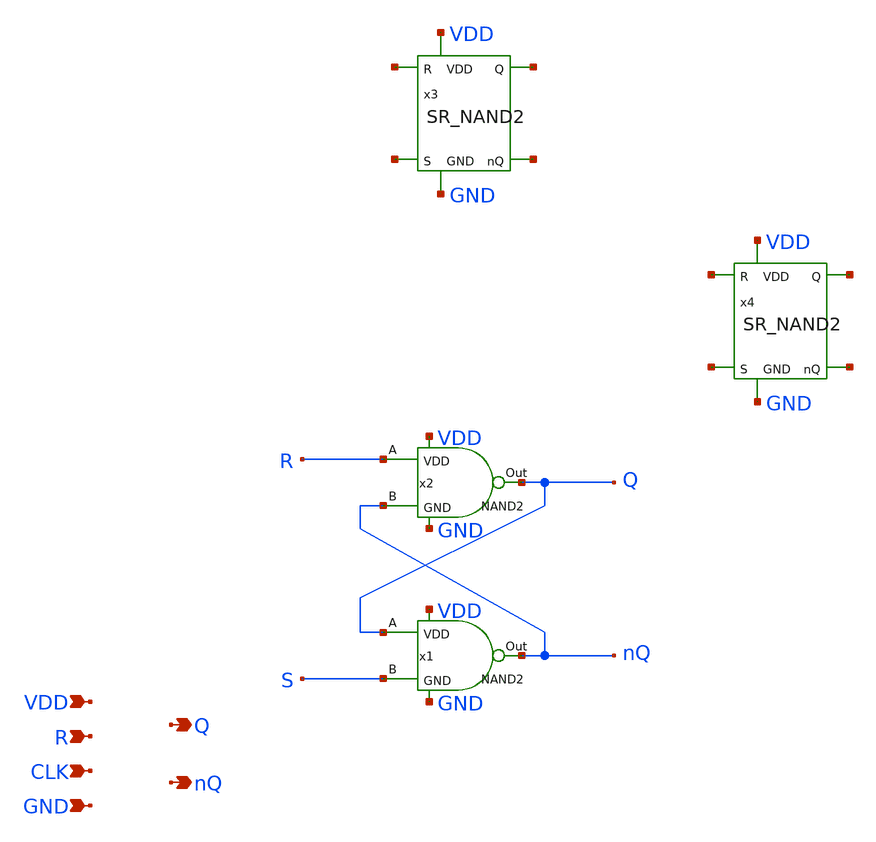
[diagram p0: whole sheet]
** sch_path: src/Dff.sch
**.subckt Dff Q R CLK VDD GND nQ
*.opin Q
*.ipin R
*.ipin CLK
*.ipin VDD
*.ipin GND
*.opin nQ
x1 Q nQ S VDD GND NAND2
x2 R Q nQ VDD GND NAND2
x3 VDD net1 net2 net3 net4 GND SR_NAND2
x4 VDD net5 net6 net7 net8 GND SR_NAND2
**** begin user architecture code

** opencircuitdesign pdks install
.lib $::SKYWATER_MODELS/sky130.lib.spice tt


**** end user architecture code
**.ends

* expanding   symbol:  /foss/designs/PLL2_4/src/NAND2.sym # of pins=5
** sym_path: src/NAND2.sym
** sch_path: src/NAND2.sch
.subckt NAND2 A Out B VDD GND
*.opin Out
*.ipin A
*.ipin B
*.ipin VDD
*.ipin GND
XM1 Out A VDD VDD sky130_fd_pr__pfet_01v8 L=1 W=1 nf=1 ad='int((1 + 1)/2) * 1 / 1 * 0.29' as='int((1 + 2)/2) * 1 / 1 * 0.29'
+ pd='2*int((1 + 1)/2) * (1 / 1 + 0.29)' ps='2*int((1 + 2)/2) * (1 / 1 + 0.29)' nrd='0.29 / 1 ' nrs='0.29 / 1 '
+ sa=0 sb=0 sd=0 mult=1 m=1
XM3 Out B VDD VDD sky130_fd_pr__pfet_01v8 L=1 W=1 nf=1 ad='int((1 + 1)/2) * 1 / 1 * 0.29' as='int((1 + 2)/2) * 1 / 1 * 0.29'
+ pd='2*int((1 + 1)/2) * (1 / 1 + 0.29)' ps='2*int((1 + 2)/2) * (1 / 1 + 0.29)' nrd='0.29 / 1 ' nrs='0.29 / 1 '
+ sa=0 sb=0 sd=0 mult=1 m=1
XM4 net1 B GND GND sky130_fd_pr__nfet_01v8 L=1 W=1 nf=1 ad='int((1 + 1)/2) * 1 / 1 * 0.29' as='int((1 + 2)/2) * 1 / 1 * 0.29'
+ pd='2*int((1 + 1)/2) * (1 / 1 + 0.29)' ps='2*int((1 + 2)/2) * (1 / 1 + 0.29)' nrd='0.29 / 1 ' nrs='0.29 / 1 '
+ sa=0 sb=0 sd=0 mult=1 m=1
XM5 Out A net1 GND sky130_fd_pr__nfet_01v8 L=1 W=1 nf=1 ad='int((1 + 1)/2) * 1 / 1 * 0.29' as='int((1 + 2)/2) * 1 / 1 * 0.29'
+ pd='2*int((1 + 1)/2) * (1 / 1 + 0.29)' ps='2*int((1 + 2)/2) * (1 / 1 + 0.29)' nrd='0.29 / 1 ' nrs='0.29 / 1 '
+ sa=0 sb=0 sd=0 mult=1 m=1
.ends


* expanding   symbol:  /foss/designs/PLL2_4/src/SR_NAND2.sym # of pins=6
** sym_path: src/SR_NAND2.sym
** sch_path: src/SR_NAND2.sch
.subckt SR_NAND2 VDD Q R S nQ GND
*.opin Q
*.ipin R
*.ipin S
*.ipin VDD
*.ipin GND
*.opin nQ
x1 Q nQ S VDD GND NAND2
x2 R Q nQ VDD GND NAND2
.ends

.end
